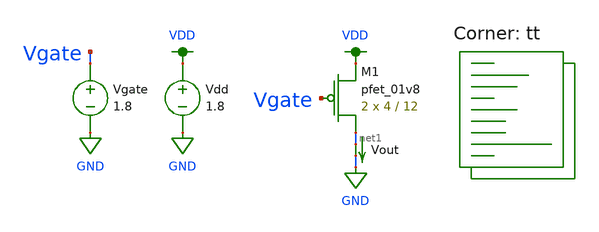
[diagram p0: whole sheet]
** sch_path: dac/schematic/2m_isat_tb.sch
**.subckt 2m_isat_tb
Vdd VDD GND 1.8
Vgate Vgate GND 1.8
Vout net1 GND 0
.save i(vout)
XM1 net1 Vgate VDD VDD sky130_fd_pr__pfet_01v8 L=12 W=4 nf=1 ad='int((nf+1)/2) * W/nf * 0.29' as='int((nf+2)/2) * W/nf * 0.29'
+ pd='2*int((nf+1)/2) * (W/nf + 0.29)' ps='2*int((nf+2)/2) * (W/nf + 0.29)' nrd='0.29 / W' nrs='0.29 / W'
+ sa=0 sb=0 sd=0 mult=2 m=2
**** begin user architecture code
.lib $::SKYWATER_MODELS/sky130.lib.spice tt

.control
  set wr_vecnames
  set wr_singlescale
  dc Vgate 0 1.8 0.01
  wrdata ~/documents/git/madvlsi/dac/build/2m_isat/2m_isat_tb.txt i(Vout)
.endc

**** end user architecture code
**.ends
.GLOBAL GND
.GLOBAL VDD
.end
